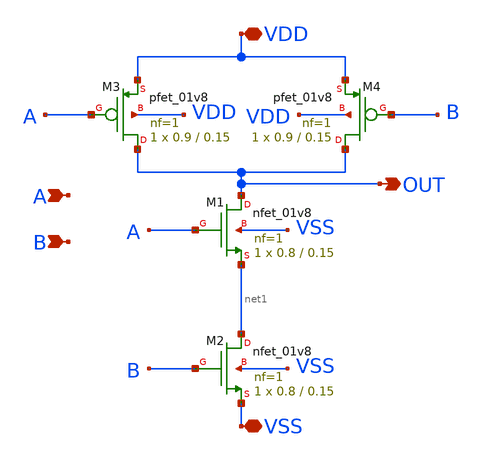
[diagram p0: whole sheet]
** sch_path: design/NAND2/xschem/nand2.sch
**.subckt nand2 VSS A B VDD OUT
*.iopin VSS
*.ipin A
*.ipin B
*.iopin VDD
*.opin OUT
XM2 net1 B VSS VSS sky130_fd_pr__nfet_01v8 L=0.15 W=0.8 nf=1 ad='int((nf+1)/2) * W/nf * 0.29' as='int((nf+2)/2) * W/nf * 0.29'
+ pd='2*int((nf+1)/2) * (W/nf + 0.29)' ps='2*int((nf+2)/2) * (W/nf + 0.29)' nrd='0.29 / W' nrs='0.29 / W'
+ sa=0 sb=0 sd=0 mult=1 m=1
XM1 OUT A net1 VSS sky130_fd_pr__nfet_01v8 L=0.15 W=0.8 nf=1 ad='int((nf+1)/2) * W/nf * 0.29' as='int((nf+2)/2) * W/nf * 0.29'
+ pd='2*int((nf+1)/2) * (W/nf + 0.29)' ps='2*int((nf+2)/2) * (W/nf + 0.29)' nrd='0.29 / W' nrs='0.29 / W'
+ sa=0 sb=0 sd=0 mult=1 m=1
XM3 OUT A VDD VDD sky130_fd_pr__pfet_01v8 L=0.15 W=0.9 nf=1 ad='int((nf+1)/2) * W/nf * 0.29' as='int((nf+2)/2) * W/nf * 0.29'
+ pd='2*int((nf+1)/2) * (W/nf + 0.29)' ps='2*int((nf+2)/2) * (W/nf + 0.29)' nrd='0.29 / W' nrs='0.29 / W'
+ sa=0 sb=0 sd=0 mult=1 m=1
XM4 OUT B VDD VDD sky130_fd_pr__pfet_01v8 L=0.15 W=0.9 nf=1 ad='int((nf+1)/2) * W/nf * 0.29' as='int((nf+2)/2) * W/nf * 0.29'
+ pd='2*int((nf+1)/2) * (W/nf + 0.29)' ps='2*int((nf+2)/2) * (W/nf + 0.29)' nrd='0.29 / W' nrs='0.29 / W'
+ sa=0 sb=0 sd=0 mult=1 m=1
**.ends
.end
